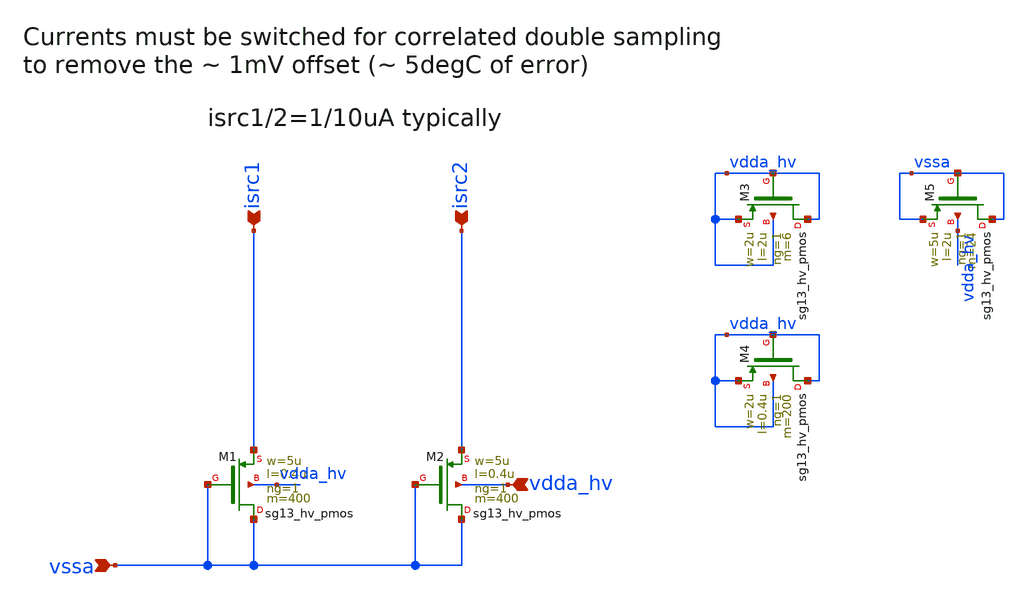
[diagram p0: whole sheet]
** sch_path: Schematics_Layout/sunrise_tsns_PMOS/sunrise_tsns_PMOS.sch
**.subckt sunrise_tsns_PMOS isrc1 isrc2 vssa vdda_hv
*.ipin isrc1
*.ipin isrc2
*.ipin vssa
*.ipin vdda_hv
XM1 vssa vssa isrc1 vdda_hv sg13_hv_pmos w=5u l=0.4u ng=1 m=400 mm_ok=1
XM2 vssa vssa isrc2 vdda_hv sg13_hv_pmos w=5u l=0.4u ng=1 m=400 mm_ok=1
XM3 vdda_hv vdda_hv vdda_hv vdda_hv sg13_hv_pmos w=2u l=2u ng=1 m=6 mm_ok=1
XM4 vdda_hv vdda_hv vdda_hv vdda_hv sg13_hv_pmos w=2u l=0.4u ng=1 m=200 mm_ok=1
XM5 vssa vssa vssa vdda_hv sg13_hv_pmos w=5u l=2u ng=1 m=24 mm_ok=1
**.ends
.end
